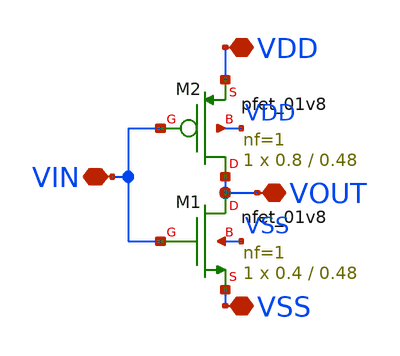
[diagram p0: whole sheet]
** sch_path: xschem/xschem_BGR_Top/Sigma_Delta/Inverter_01/Inverter_01.sch
**.subckt Inverter_01 VIN VDD VSS VOUT
*.iopin VIN
*.iopin VDD
*.iopin VSS
*.iopin VOUT
XM1 VOUT VIN VSS VSS sky130_fd_pr__nfet_01v8 L=0.48 W=0.4 nf=1 ad='int((nf+1)/2) * W/nf * 0.29' as='int((nf+2)/2) * W/nf * 0.29'
+ pd='2*int((nf+1)/2) * (W/nf + 0.29)' ps='2*int((nf+2)/2) * (W/nf + 0.29)' nrd='0.29 / W' nrs='0.29 / W'
+ sa=0 sb=0 sd=0 mult=1 m=1
XM2 VOUT VIN VDD VDD sky130_fd_pr__pfet_01v8 L=0.48 W=0.8 nf=1 ad='int((nf+1)/2) * W/nf * 0.29' as='int((nf+2)/2) * W/nf * 0.29'
+ pd='2*int((nf+1)/2) * (W/nf + 0.29)' ps='2*int((nf+2)/2) * (W/nf + 0.29)' nrd='0.29 / W' nrs='0.29 / W'
+ sa=0 sb=0 sd=0 mult=1 m=1
**** begin user architecture code

** opencircuitdesign pdks install
.lib $::SKYWATER_MODELS/sky130.lib.spice tt


**** end user architecture code
**.ends
.end
